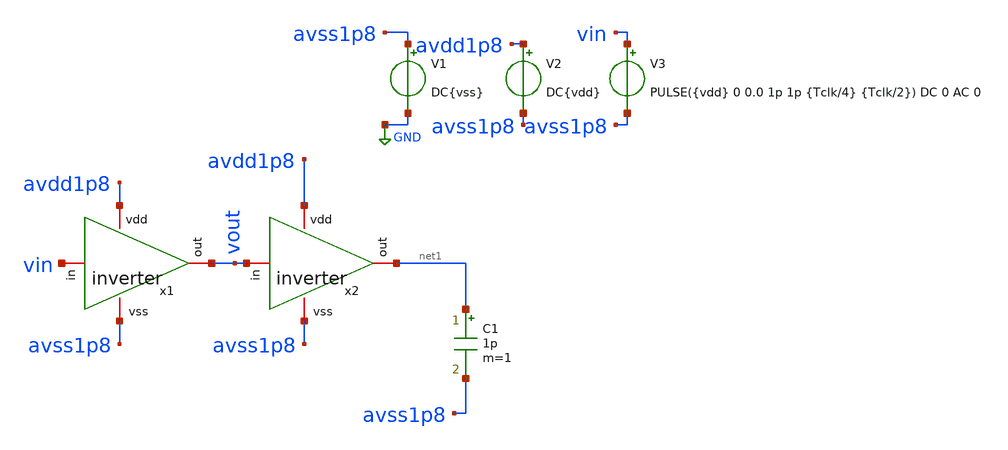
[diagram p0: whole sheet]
** sch_path: simbolos y esquematicos/tb_inverter.sch
**.subckt tb_inverter
x1 avdd1p8 vin vout avss1p8 inverter
x2 avdd1p8 vout net1 avss1p8 inverter
V1 avss1p8 GND DC{vss}
V2 avdd1p8 avss1p8 DC{vdd}
V3 vin avss1p8 PULSE({vdd} 0 0.0 1p 1p {Tclk/4} {Tclk/2}) DC 0 AC 0
C1 net1 avss1p8 1p m=1
**** begin user architecture code


* Circuit Parameters
.param vdd= 1.8
.param vss= 0.0
.param Tclk = 10n
.options TEMP = 65.0
* Include Models
.lib /foss/pdks/sky130A/libs.tech/ngspice/sky130.lib.spice TT
* OP Parameters & Singals to save
.save all
*Simulations
.control
tran 0.01u 100n
setplot tran1
plot v(vin) v(vout)+2
reset
dc V3 0 1.8 0.01
setplot dc
plot vin vout ylabel vout xlabel vin
set filetype = ascii
write dcsweep.raw
.endc
.end


**** end user architecture code
**.ends
.GLOBAL GND
.end
